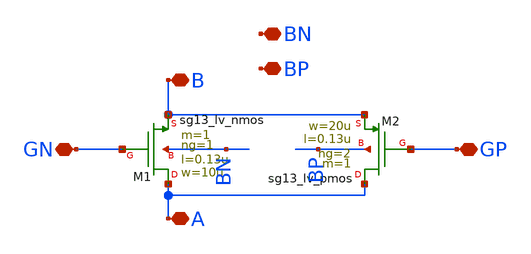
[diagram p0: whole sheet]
** sch_path: design_data/transmission_gate.sch
**.subckt transmission_gate B GN A GP BN BP
*.iopin B
*.iopin GN
*.iopin A
*.iopin GP
*.iopin BN
*.iopin BP
XM1 A GN B BN sg13_lv_nmos w=10u l=0.13u ng=1 m=1 mm_ok=1
XM2 A GP B BP sg13_lv_pmos w=20u l=0.13u ng=2 m=1 mm_ok=1
**.ends
.end
